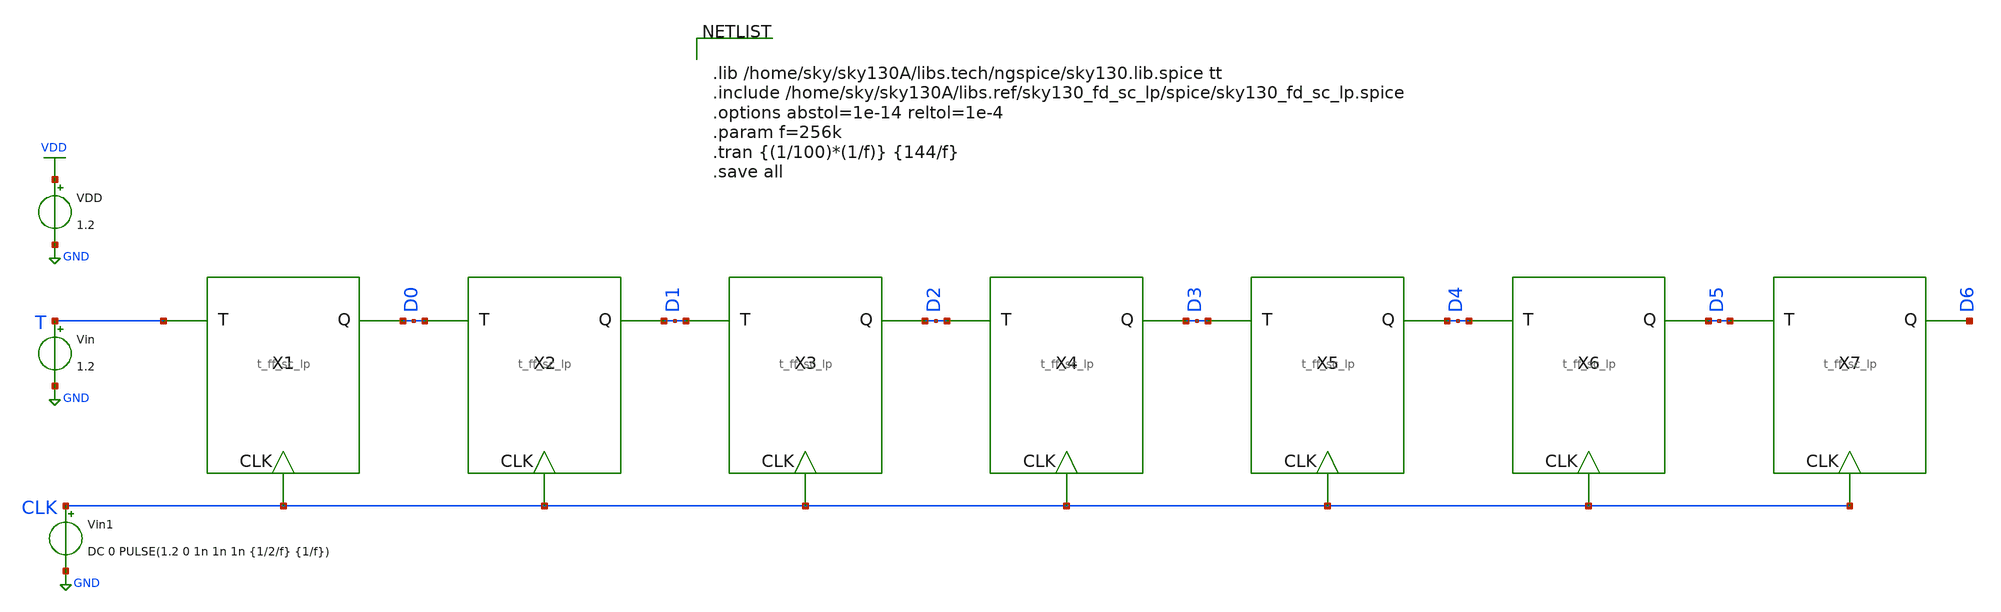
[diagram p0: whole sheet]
** sch_path: xschem/8_bit_bin_ctr/8_bit_bin_ctr.sch
**.subckt 8_bit_bin_ctr
X1 T D0 CLK t_ff_sc_lp
VDD VDD GND 1.2
Vin T GND 1.2
Vin1 CLK GND DC 0 PULSE(1.2 0 1n 1n 1n {1/2/f} {1/f})
X2 D0 D1 CLK t_ff_sc_lp
X3 D1 D2 CLK t_ff_sc_lp
X4 D2 D3 CLK t_ff_sc_lp
X5 D3 D4 CLK t_ff_sc_lp
X6 D4 D5 CLK t_ff_sc_lp
X7 D5 D6 CLK t_ff_sc_lp
**** begin user architecture code


.lib /home/sky/sky130A/libs.tech/ngspice/sky130.lib.spice tt
.include /home/sky/sky130A/libs.ref/sky130_fd_sc_lp/spice/sky130_fd_sc_lp.spice
.options abstol=1e-14 reltol=1e-4
.param f=256k
.tran {(1/100)*(1/f)} {144/f}
.save all


**** end user architecture code
**.ends

* expanding   symbol:  T_flip_flop/t_ff_sc_lp.sym # of pins=3
** sym_path: T_flip_flop/t_ff_sc_lp.sym
** sch_path: T_flip_flop/t_ff_sc_lp.sch
.subckt t_ff_sc_lp T Q CLK
*.ipin T
*.ipin CLK
*.opin Q
x3 Q T GND GND VDD VDD net1 sky130_fd_sc_lp__xor2_1
x1 CLK net1 GND GND VDD VDD Q sky130_fd_sc_lp__dfxtp_1
.ends

.GLOBAL VDD
.GLOBAL GND
.end
